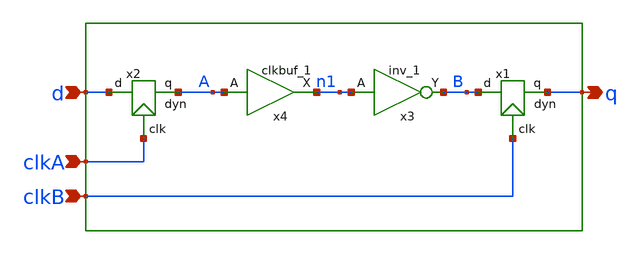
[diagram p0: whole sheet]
** sch_path: src/xe/test_cases/dyn_dyn_odd.sch
**.subckt dyn_dyn_odd d clkA q clkB
*.ipin d
*.ipin clkA
*.opin q
*.ipin clkB
x2 clkA A d dyn
x4 A vss vss vcc vcc n1 sky130_fd_sc_hd__clkbuf_1
x1 clkB q B dyn
x3 n1 vss vss vcc vcc B sky130_fd_sc_hd__inv_1
**.ends

* expanding   symbol:  yxt/dyn.sym # of pins=3
** sym_path: src/xe/test_cases/dyn.sym
** sch_path: src/xe/test_cases/dyn.sch
.subckt dyn clk q d
*.ipin clk
*.opin q
*.ipin d
x1 z vss vss vcc vcc q sky130_fd_sc_hd__inv_1
XM1 z d net1 vss sky130_fd_pr__nfet_01v8 L=0.15 W=1 nf=1 ad='int((nf+1)/2) * W/nf * 0.29' as='int((nf+2)/2) * W/nf * 0.29'
+ pd='2*int((nf+1)/2) * (W/nf + 0.29)' ps='2*int((nf+2)/2) * (W/nf + 0.29)' nrd='0.29 / W' nrs='0.29 / W'
+ sa=0 sb=0 sd=0 mult=1 m=1
XM2 z q vcc vcc sky130_fd_pr__pfet_01v8 L=0.15 W=1 nf=1 ad='int((nf+1)/2) * W/nf * 0.29' as='int((nf+2)/2) * W/nf * 0.29'
+ pd='2*int((nf+1)/2) * (W/nf + 0.29)' ps='2*int((nf+2)/2) * (W/nf + 0.29)' nrd='0.29 / W' nrs='0.29 / W'
+ sa=0 sb=0 sd=0 mult=1 m=1
XM3 z clk vcc vcc sky130_fd_pr__pfet_01v8 L=0.15 W=1 nf=1 ad='int((nf+1)/2) * W/nf * 0.29' as='int((nf+2)/2) * W/nf * 0.29'
+ pd='2*int((nf+1)/2) * (W/nf + 0.29)' ps='2*int((nf+2)/2) * (W/nf + 0.29)' nrd='0.29 / W' nrs='0.29 / W'
+ sa=0 sb=0 sd=0 mult=1 m=1
XM4 net1 clk vss vss sky130_fd_pr__nfet_01v8 L=0.15 W=1 nf=1 ad='int((nf+1)/2) * W/nf * 0.29' as='int((nf+2)/2) * W/nf * 0.29'
+ pd='2*int((nf+1)/2) * (W/nf + 0.29)' ps='2*int((nf+2)/2) * (W/nf + 0.29)' nrd='0.29 / W' nrs='0.29 / W'
+ sa=0 sb=0 sd=0 mult=1 m=1
.ends

.end
